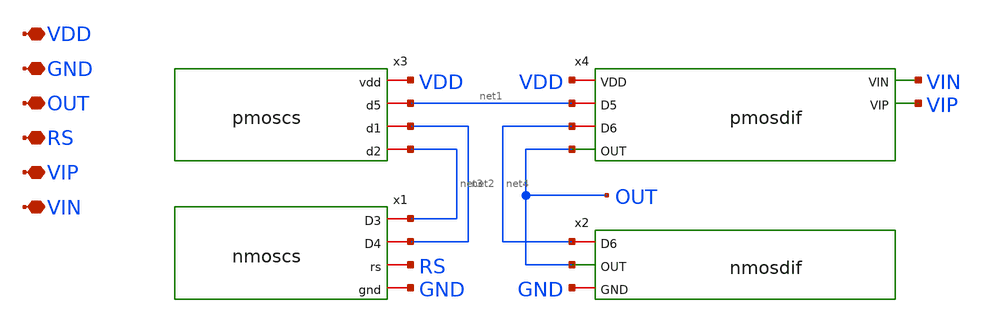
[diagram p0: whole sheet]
** sch_path: OPAMP/mag/opamp.sch
**.subckt opamp VDD GND OUT RS VIP VIN
*.iopin VDD
*.iopin GND
*.iopin OUT
*.iopin RS
*.iopin VIP
*.iopin VIN
x1 net3 net2 RS GND nmoscs
x2 net4 OUT GND nmosdif
x3 VDD net1 net2 net3 pmoscs
x4 VDD net1 VIN VIP net4 OUT pmosdif
**.ends
.end
